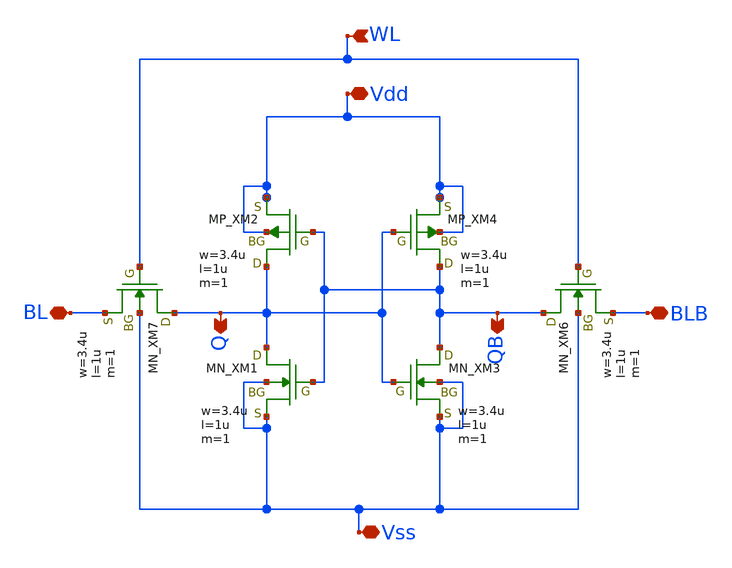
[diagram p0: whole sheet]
** sch_path: sram.sch
**.subckt sram Vdd Vss BLB BL WL Q QB
*.iopin Vdd
*.iopin Vss
*.iopin BLB
*.iopin BL
*.ipin WL
*.opin Q
*.opin QB
XXM1 Q QB Vss Vss NMOS w=3.4u l=1u nrd=0 nrs=0 m=1
XXM2 Q QB Vdd Vdd PMOS w=3.4u l=1u nrd=0 nrs=0 m=1
XXM3 QB Q Vss Vss NMOS w=3.4u l=1u nrd=0 nrs=0 m=1
XXM4 QB Q Vdd Vdd PMOS w=3.4u l=1u nrd=0 nrs=0 m=1
XXM7 Q WL BL Vss NMOS w=3.4u l=1u nrd=0 nrs=0 m=1
XXM6 QB WL BLB Vss NMOS w=3.4u l=1u nrd=0 nrs=0 m=1
**.ends
.end
